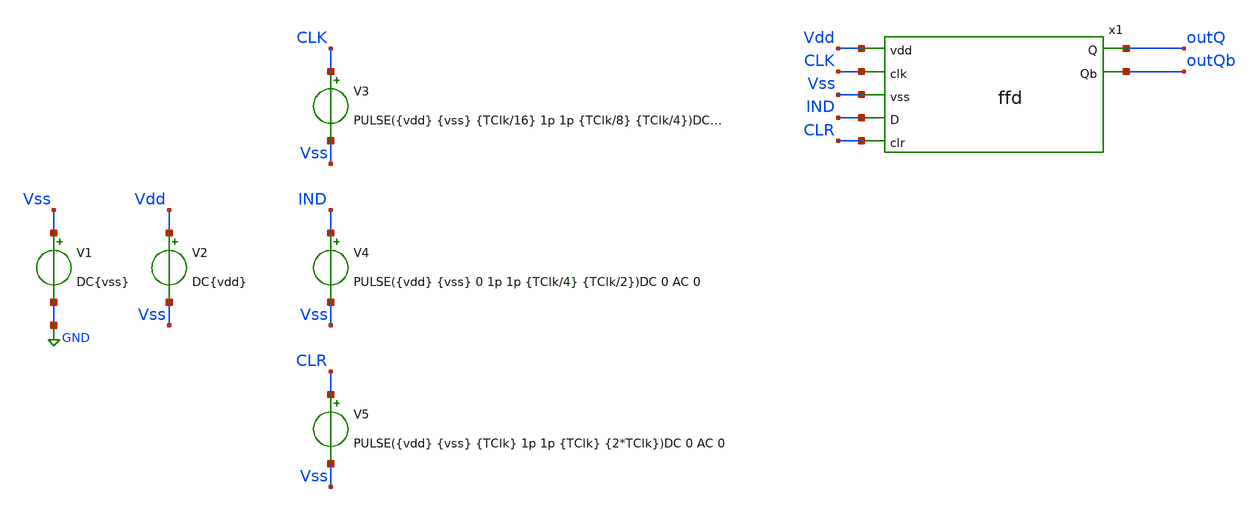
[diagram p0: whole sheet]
** sch_path: icdesign/sch/FFD/tb_ffd.sch
**.subckt tb_ffd
V1 Vss GND DC{vss}
V2 Vdd Vss DC{vdd}
V3 CLK Vss PULSE({vdd} {vss} {TClk/16} 1p 1p {TClk/8} {TClk/4})DC 0 AC 0
V4 IND Vss PULSE({vdd} {vss} 0 1p 1p {TClk/4} {TClk/2})DC 0 AC 0
V5 CLR Vss PULSE({vdd} {vss} {TClk} 1p 1p {TClk} {2*TClk})DC 0 AC 0
x1 Vdd CLK Vss outQ IND outQb CLR ffd
**** begin user architecture code





* Circuit Parameters
.param vdd  = 1.8
.param vss  = 0.0
.param Tclk = 10n
.options TEMP = 65.0


* Include Models
.lib ~/skywater/skywater-pdk/libraries/sky130_fd_pr_ngspice/latest/models/corners/sky130.lib TT


* OP Parameters & Singals to save
.save all


*Simulations
.control
  tran 0.01u 20n
  setplot tran1
  plot v(CLK)v(CLR)+2 v(IND)+4 v(outQ)+6 v(outQB)+8
.endc
.end


**** end user architecture code
**.ends
.GLOBAL GND
.end
